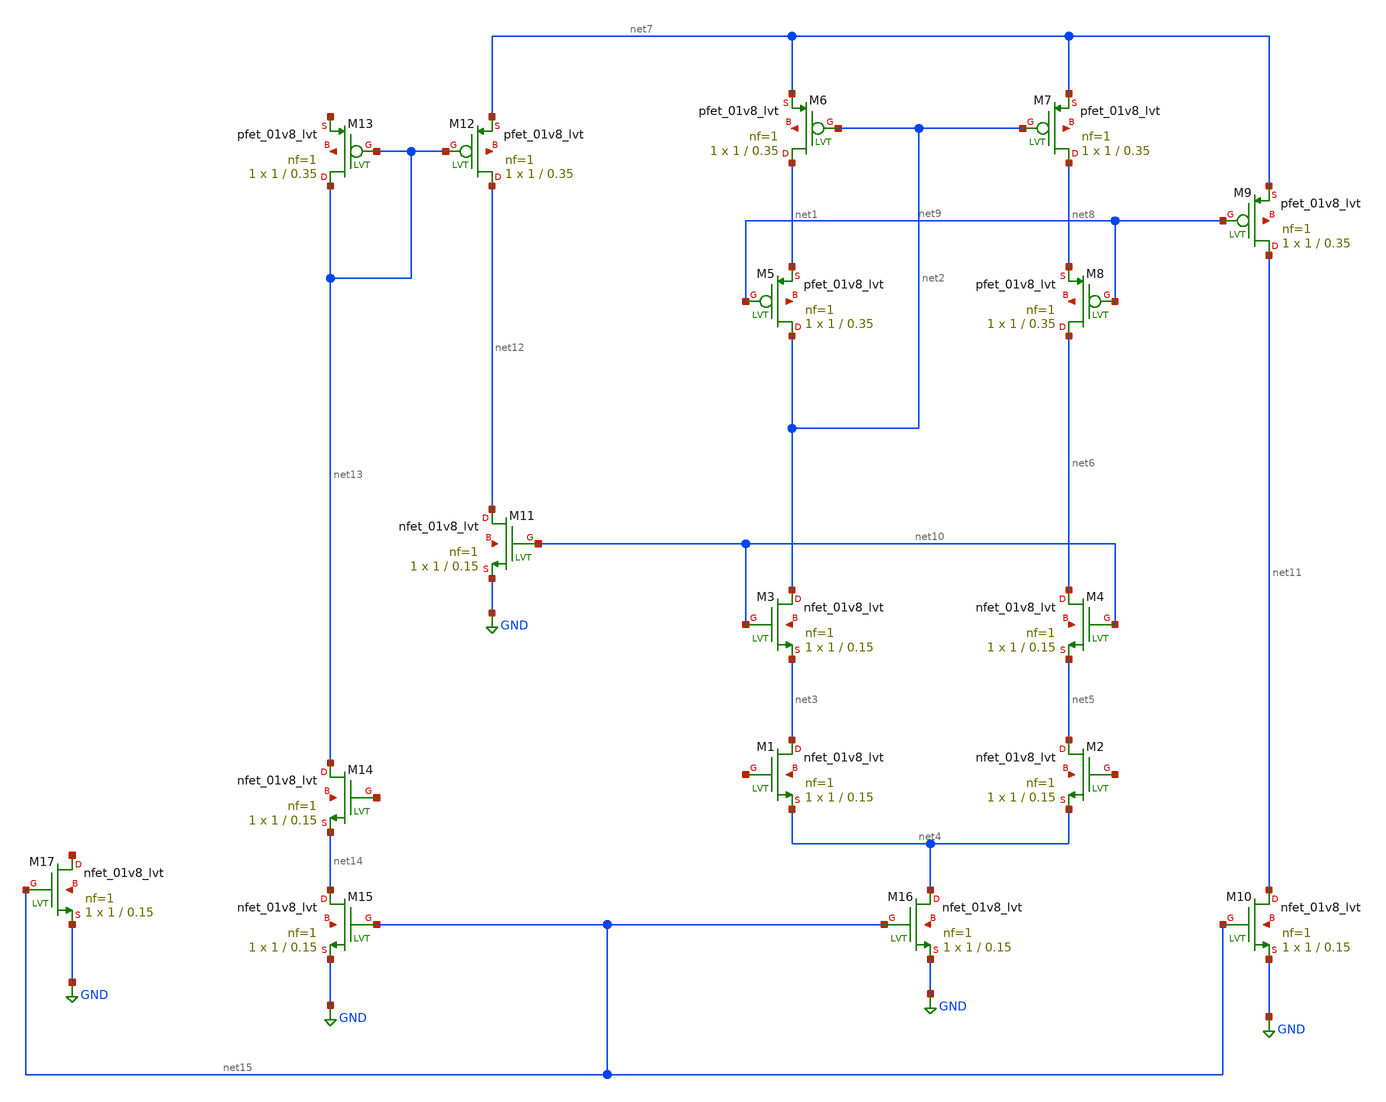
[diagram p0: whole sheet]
** sch_path: Work/xschem/telescopic_vcvs.sch
**.subckt telescopic_vcvs
XM1 net3 net16 net4 net17 sky130_fd_pr__nfet_01v8_lvt L=0.15 W=1 nf=1 ad='int((1 + 1)/2) * 1 / 1 * 0.29'
+ as='int((1 + 2)/2) * 1 / 1 * 0.29' pd='2*int((1 + 1)/2) * (1 / 1 + 0.29)' ps='2*int((1 + 2)/2) * (1 / 1 + 0.29)'
+ nrd='0.29 / 1 ' nrs='0.29 / 1 ' sa=0 sb=0 sd=0 mult=1 m=1
XM2 net5 net18 net4 net19 sky130_fd_pr__nfet_01v8_lvt L=0.15 W=1 nf=1 ad='int((1 + 1)/2) * 1 / 1 * 0.29'
+ as='int((1 + 2)/2) * 1 / 1 * 0.29' pd='2*int((1 + 1)/2) * (1 / 1 + 0.29)' ps='2*int((1 + 2)/2) * (1 / 1 + 0.29)'
+ nrd='0.29 / 1 ' nrs='0.29 / 1 ' sa=0 sb=0 sd=0 mult=1 m=1
XM3 net2 net10 net3 net20 sky130_fd_pr__nfet_01v8_lvt L=0.15 W=1 nf=1 ad='int((1 + 1)/2) * 1 / 1 * 0.29'
+ as='int((1 + 2)/2) * 1 / 1 * 0.29' pd='2*int((1 + 1)/2) * (1 / 1 + 0.29)' ps='2*int((1 + 2)/2) * (1 / 1 + 0.29)'
+ nrd='0.29 / 1 ' nrs='0.29 / 1 ' sa=0 sb=0 sd=0 mult=1 m=1
XM4 net6 net10 net5 net21 sky130_fd_pr__nfet_01v8_lvt L=0.15 W=1 nf=1 ad='int((1 + 1)/2) * 1 / 1 * 0.29'
+ as='int((1 + 2)/2) * 1 / 1 * 0.29' pd='2*int((1 + 1)/2) * (1 / 1 + 0.29)' ps='2*int((1 + 2)/2) * (1 / 1 + 0.29)'
+ nrd='0.29 / 1 ' nrs='0.29 / 1 ' sa=0 sb=0 sd=0 mult=1 m=1
XM5 net2 net9 net1 net22 sky130_fd_pr__pfet_01v8_lvt L=0.35 W=1 nf=1 ad='int((1 + 1)/2) * 1 / 1 * 0.29'
+ as='int((1 + 2)/2) * 1 / 1 * 0.29' pd='2*int((1 + 1)/2) * (1 / 1 + 0.29)' ps='2*int((1 + 2)/2) * (1 / 1 + 0.29)'
+ nrd='0.29 / 1 ' nrs='0.29 / 1 ' sa=0 sb=0 sd=0 mult=1 m=1
XM6 net1 net2 net7 net23 sky130_fd_pr__pfet_01v8_lvt L=0.35 W=1 nf=1 ad='int((1 + 1)/2) * 1 / 1 * 0.29'
+ as='int((1 + 2)/2) * 1 / 1 * 0.29' pd='2*int((1 + 1)/2) * (1 / 1 + 0.29)' ps='2*int((1 + 2)/2) * (1 / 1 + 0.29)'
+ nrd='0.29 / 1 ' nrs='0.29 / 1 ' sa=0 sb=0 sd=0 mult=1 m=1
XM7 net8 net2 net7 net24 sky130_fd_pr__pfet_01v8_lvt L=0.35 W=1 nf=1 ad='int((1 + 1)/2) * 1 / 1 * 0.29'
+ as='int((1 + 2)/2) * 1 / 1 * 0.29' pd='2*int((1 + 1)/2) * (1 / 1 + 0.29)' ps='2*int((1 + 2)/2) * (1 / 1 + 0.29)'
+ nrd='0.29 / 1 ' nrs='0.29 / 1 ' sa=0 sb=0 sd=0 mult=1 m=1
XM8 net6 net9 net8 net25 sky130_fd_pr__pfet_01v8_lvt L=0.35 W=1 nf=1 ad='int((1 + 1)/2) * 1 / 1 * 0.29'
+ as='int((1 + 2)/2) * 1 / 1 * 0.29' pd='2*int((1 + 1)/2) * (1 / 1 + 0.29)' ps='2*int((1 + 2)/2) * (1 / 1 + 0.29)'
+ nrd='0.29 / 1 ' nrs='0.29 / 1 ' sa=0 sb=0 sd=0 mult=1 m=1
XM9 net11 net9 net7 net26 sky130_fd_pr__pfet_01v8_lvt L=0.35 W=1 nf=1 ad='int((1 + 1)/2) * 1 / 1 * 0.29'
+ as='int((1 + 2)/2) * 1 / 1 * 0.29' pd='2*int((1 + 1)/2) * (1 / 1 + 0.29)' ps='2*int((1 + 2)/2) * (1 / 1 + 0.29)'
+ nrd='0.29 / 1 ' nrs='0.29 / 1 ' sa=0 sb=0 sd=0 mult=1 m=1
XM10 net11 net15 GND net27 sky130_fd_pr__nfet_01v8_lvt L=0.15 W=1 nf=1 ad='int((1 + 1)/2) * 1 / 1 * 0.29'
+ as='int((1 + 2)/2) * 1 / 1 * 0.29' pd='2*int((1 + 1)/2) * (1 / 1 + 0.29)' ps='2*int((1 + 2)/2) * (1 / 1 + 0.29)'
+ nrd='0.29 / 1 ' nrs='0.29 / 1 ' sa=0 sb=0 sd=0 mult=1 m=1
XM11 net12 net10 GND net28 sky130_fd_pr__nfet_01v8_lvt L=0.15 W=1 nf=1 ad='int((1 + 1)/2) * 1 / 1 * 0.29'
+ as='int((1 + 2)/2) * 1 / 1 * 0.29' pd='2*int((1 + 1)/2) * (1 / 1 + 0.29)' ps='2*int((1 + 2)/2) * (1 / 1 + 0.29)'
+ nrd='0.29 / 1 ' nrs='0.29 / 1 ' sa=0 sb=0 sd=0 mult=1 m=1
XM12 net12 net13 net7 net29 sky130_fd_pr__pfet_01v8_lvt L=0.35 W=1 nf=1 ad='int((1 + 1)/2) * 1 / 1 * 0.29'
+ as='int((1 + 2)/2) * 1 / 1 * 0.29' pd='2*int((1 + 1)/2) * (1 / 1 + 0.29)' ps='2*int((1 + 2)/2) * (1 / 1 + 0.29)'
+ nrd='0.29 / 1 ' nrs='0.29 / 1 ' sa=0 sb=0 sd=0 mult=1 m=1
XM13 net13 net13 net30 net31 sky130_fd_pr__pfet_01v8_lvt L=0.35 W=1 nf=1 ad='int((1 + 1)/2) * 1 / 1 * 0.29'
+ as='int((1 + 2)/2) * 1 / 1 * 0.29' pd='2*int((1 + 1)/2) * (1 / 1 + 0.29)' ps='2*int((1 + 2)/2) * (1 / 1 + 0.29)'
+ nrd='0.29 / 1 ' nrs='0.29 / 1 ' sa=0 sb=0 sd=0 mult=1 m=1
XM14 net13 net32 net14 net33 sky130_fd_pr__nfet_01v8_lvt L=0.15 W=1 nf=1 ad='int((1 + 1)/2) * 1 / 1 * 0.29'
+ as='int((1 + 2)/2) * 1 / 1 * 0.29' pd='2*int((1 + 1)/2) * (1 / 1 + 0.29)' ps='2*int((1 + 2)/2) * (1 / 1 + 0.29)'
+ nrd='0.29 / 1 ' nrs='0.29 / 1 ' sa=0 sb=0 sd=0 mult=1 m=1
XM15 net14 net15 GND net34 sky130_fd_pr__nfet_01v8_lvt L=0.15 W=1 nf=1 ad='int((1 + 1)/2) * 1 / 1 * 0.29'
+ as='int((1 + 2)/2) * 1 / 1 * 0.29' pd='2*int((1 + 1)/2) * (1 / 1 + 0.29)' ps='2*int((1 + 2)/2) * (1 / 1 + 0.29)'
+ nrd='0.29 / 1 ' nrs='0.29 / 1 ' sa=0 sb=0 sd=0 mult=1 m=1
XM16 net4 net15 GND net35 sky130_fd_pr__nfet_01v8_lvt L=0.15 W=1 nf=1 ad='int((1 + 1)/2) * 1 / 1 * 0.29'
+ as='int((1 + 2)/2) * 1 / 1 * 0.29' pd='2*int((1 + 1)/2) * (1 / 1 + 0.29)' ps='2*int((1 + 2)/2) * (1 / 1 + 0.29)'
+ nrd='0.29 / 1 ' nrs='0.29 / 1 ' sa=0 sb=0 sd=0 mult=1 m=1
XM17 net36 net15 GND net37 sky130_fd_pr__nfet_01v8_lvt L=0.15 W=1 nf=1 ad='int((1 + 1)/2) * 1 / 1 * 0.29'
+ as='int((1 + 2)/2) * 1 / 1 * 0.29' pd='2*int((1 + 1)/2) * (1 / 1 + 0.29)' ps='2*int((1 + 2)/2) * (1 / 1 + 0.29)'
+ nrd='0.29 / 1 ' nrs='0.29 / 1 ' sa=0 sb=0 sd=0 mult=1 m=1
**.ends
.GLOBAL GND
.end
